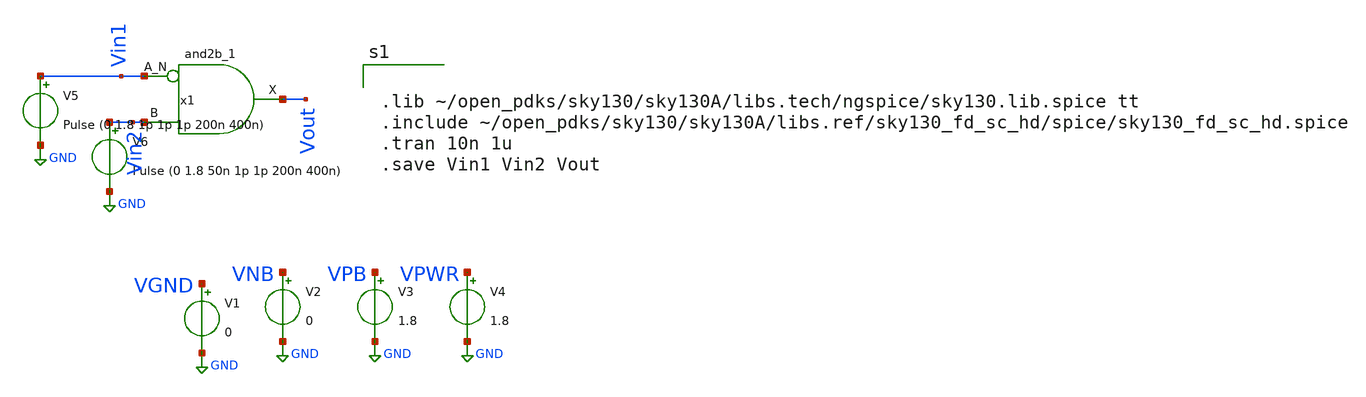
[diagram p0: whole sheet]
** sch_path: clks.sch
**.subckt clks
x1 Vin1 Vin2 VGND VNB VPB VPWR Vout sky130_fd_sc_hd__and2b_1
V1 VGND GND 0
V2 VNB GND 0
V3 VPB GND 1.8
V4 VPWR GND 1.8
V5 Vin1 GND Pulse (0 1.8 1p 1p 1p 200n 400n)
V6 Vin2 GND Pulse (0 1.8 50n 1p 1p 200n 400n)
**** begin user architecture code


.lib ~/open_pdks/sky130/sky130A/libs.tech/ngspice/sky130.lib.spice tt
.include ~/open_pdks/sky130/sky130A/libs.ref/sky130_fd_sc_hd/spice/sky130_fd_sc_hd.spice
.tran 10n 1u
.save Vin1 Vin2 Vout

**** end user architecture code
**.ends
.GLOBAL GND
.end
